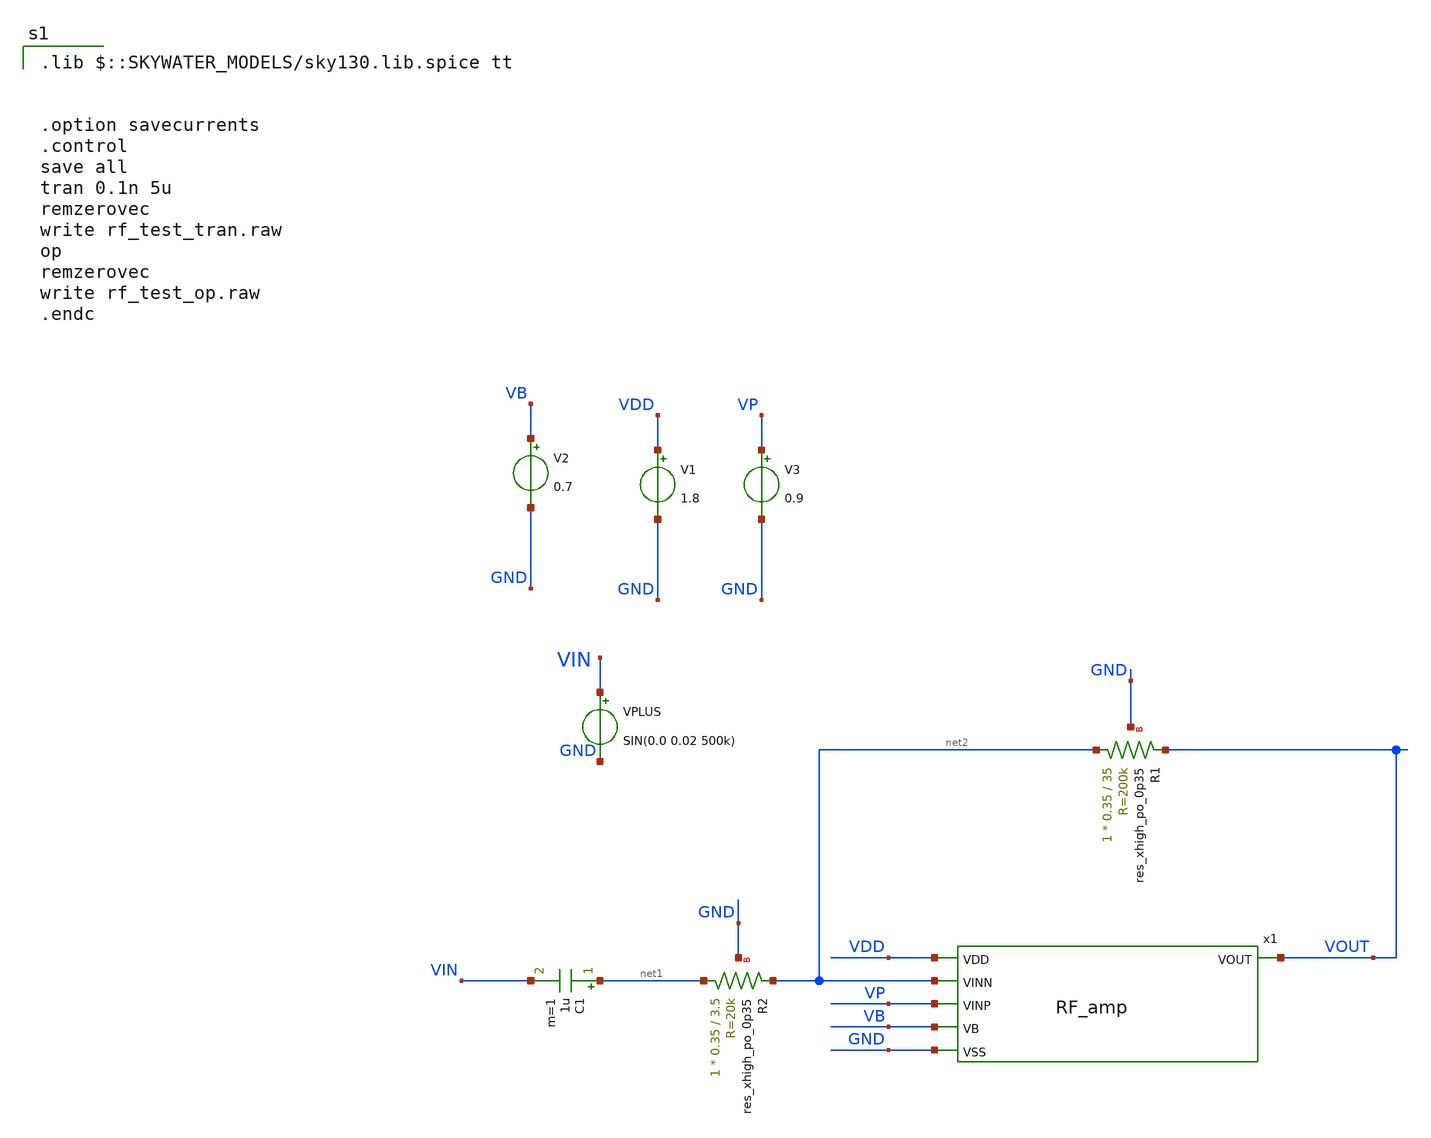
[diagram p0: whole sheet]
** sch_path: xschem/RF_amp_test.sch
**.subckt RF_amp_test
V1 VDD GND 1.8
VPLUS VIN GND SIN(0.0 0.02 500k)
x1 VDD net2 VOUT VP VB GND RF_amp
V2 VB GND 0.7
XR1 net2 VOUT GND sky130_fd_pr__res_xhigh_po_0p35 L=35 mult=1 m=1
XR2 net1 net2 GND sky130_fd_pr__res_xhigh_po_0p35 L=3.5 mult=1 m=1
V3 VP GND 0.9
C1 net1 VIN 1u m=1
**** begin user architecture code
 .lib $::SKYWATER_MODELS/sky130.lib.spice tt


.option savecurrents
.control
save all
tran 0.1n 5u
remzerovec
write rf_test_tran.raw
op
remzerovec
write rf_test_op.raw
.endc



**** end user architecture code
**.ends

* expanding   symbol:  RF_amp.sym # of pins=6
** sym_path: xschem/RF_amp.sym
** sch_path: xschem/RF_amp.sch
.subckt RF_amp VDD VINN VOUT VINP VB VSS
*.ipin VDD
*.ipin VINN
*.ipin VINP
*.ipin VB
*.ipin VSS
*.opin VOUT
XM1 net3 VINN net4 VSS sky130_fd_pr__nfet_01v8_lvt L=1 W=50 nf=1 ad='int((nf+1)/2) * W/nf * 0.29' as='int((nf+2)/2) * W/nf * 0.29'
+ pd='2*int((nf+1)/2) * (W/nf + 0.29)' ps='2*int((nf+2)/2) * (W/nf + 0.29)' nrd='0.29 / W' nrs='0.29 / W'
+ sa=0 sb=0 sd=0 mult=1 m=1
XM2 net2 VINP net4 VSS sky130_fd_pr__nfet_01v8_lvt L=1 W=50 nf=1 ad='int((nf+1)/2) * W/nf * 0.29' as='int((nf+2)/2) * W/nf * 0.29'
+ pd='2*int((nf+1)/2) * (W/nf + 0.29)' ps='2*int((nf+2)/2) * (W/nf + 0.29)' nrd='0.29 / W' nrs='0.29 / W'
+ sa=0 sb=0 sd=0 mult=1 m=1
XM5 net3 net3 VDD VDD sky130_fd_pr__pfet_01v8 L=1 W=10 nf=1 ad='int((nf+1)/2) * W/nf * 0.29' as='int((nf+2)/2) * W/nf * 0.29'
+ pd='2*int((nf+1)/2) * (W/nf + 0.29)' ps='2*int((nf+2)/2) * (W/nf + 0.29)' nrd='0.29 / W' nrs='0.29 / W'
+ sa=0 sb=0 sd=0 mult=1 m=1
XM6 net2 net3 VDD VDD sky130_fd_pr__pfet_01v8 L=1 W=10 nf=1 ad='int((nf+1)/2) * W/nf * 0.29' as='int((nf+2)/2) * W/nf * 0.29'
+ pd='2*int((nf+1)/2) * (W/nf + 0.29)' ps='2*int((nf+2)/2) * (W/nf + 0.29)' nrd='0.29 / W' nrs='0.29 / W'
+ sa=0 sb=0 sd=0 mult=1 m=1
XM7 VOUT net2 VDD VDD sky130_fd_pr__pfet_01v8 L=1 W=20 nf=1 ad='int((nf+1)/2) * W/nf * 0.29' as='int((nf+2)/2) * W/nf * 0.29'
+ pd='2*int((nf+1)/2) * (W/nf + 0.29)' ps='2*int((nf+2)/2) * (W/nf + 0.29)' nrd='0.29 / W' nrs='0.29 / W'
+ sa=0 sb=0 sd=0 mult=1 m=1
XR1 net1 net2 VSS sky130_fd_pr__res_xhigh_po_0p35 L=1 mult=1 m=1
XC1 net1 VOUT sky130_fd_pr__cap_mim_m3_2 W=20 L=20 MF=1 m=1
XM3 net4 VB VSS VSS sky130_fd_pr__nfet_01v8 L=1 W=10 nf=1 ad='int((nf+1)/2) * W/nf * 0.29' as='int((nf+2)/2) * W/nf * 0.29'
+ pd='2*int((nf+1)/2) * (W/nf + 0.29)' ps='2*int((nf+2)/2) * (W/nf + 0.29)' nrd='0.29 / W' nrs='0.29 / W'
+ sa=0 sb=0 sd=0 mult=1 m=1
XM4 VOUT VB VSS VSS sky130_fd_pr__nfet_01v8 L=1 W=10 nf=1 ad='int((nf+1)/2) * W/nf * 0.29' as='int((nf+2)/2) * W/nf * 0.29'
+ pd='2*int((nf+1)/2) * (W/nf + 0.29)' ps='2*int((nf+2)/2) * (W/nf + 0.29)' nrd='0.29 / W' nrs='0.29 / W'
+ sa=0 sb=0 sd=0 mult=1 m=1
.ends

.end
